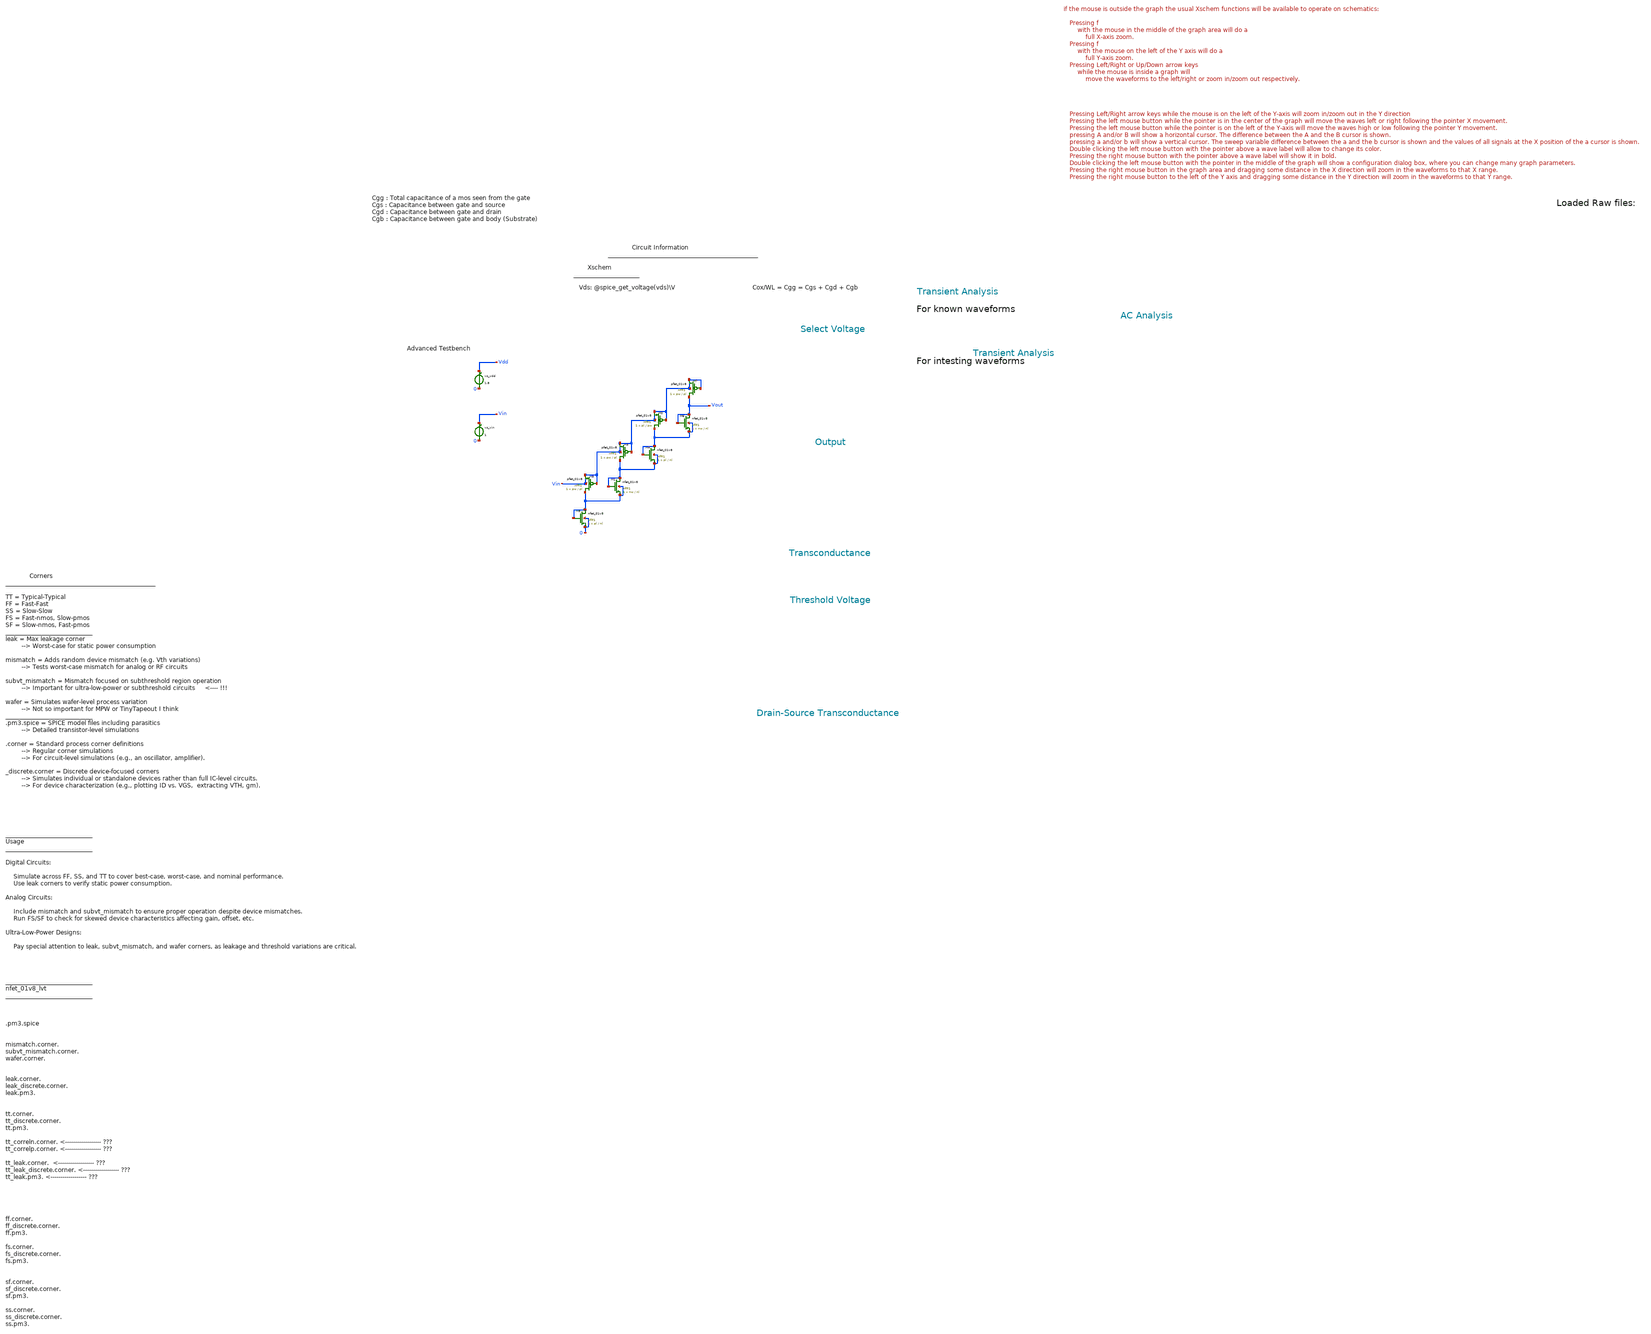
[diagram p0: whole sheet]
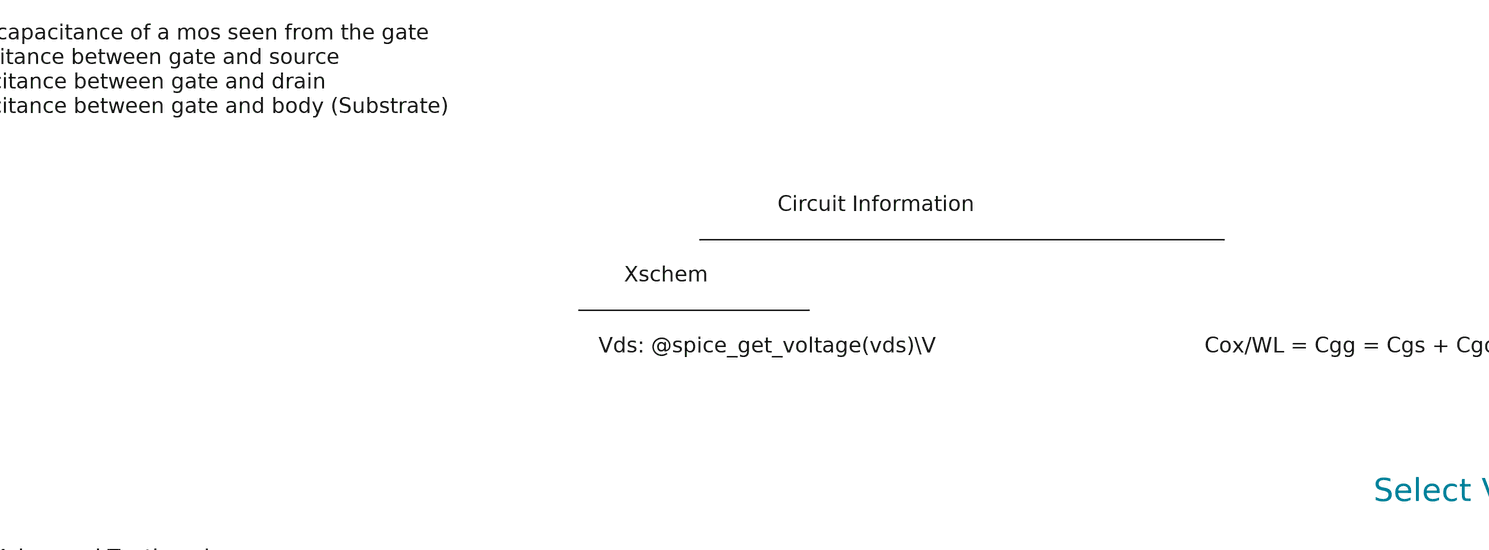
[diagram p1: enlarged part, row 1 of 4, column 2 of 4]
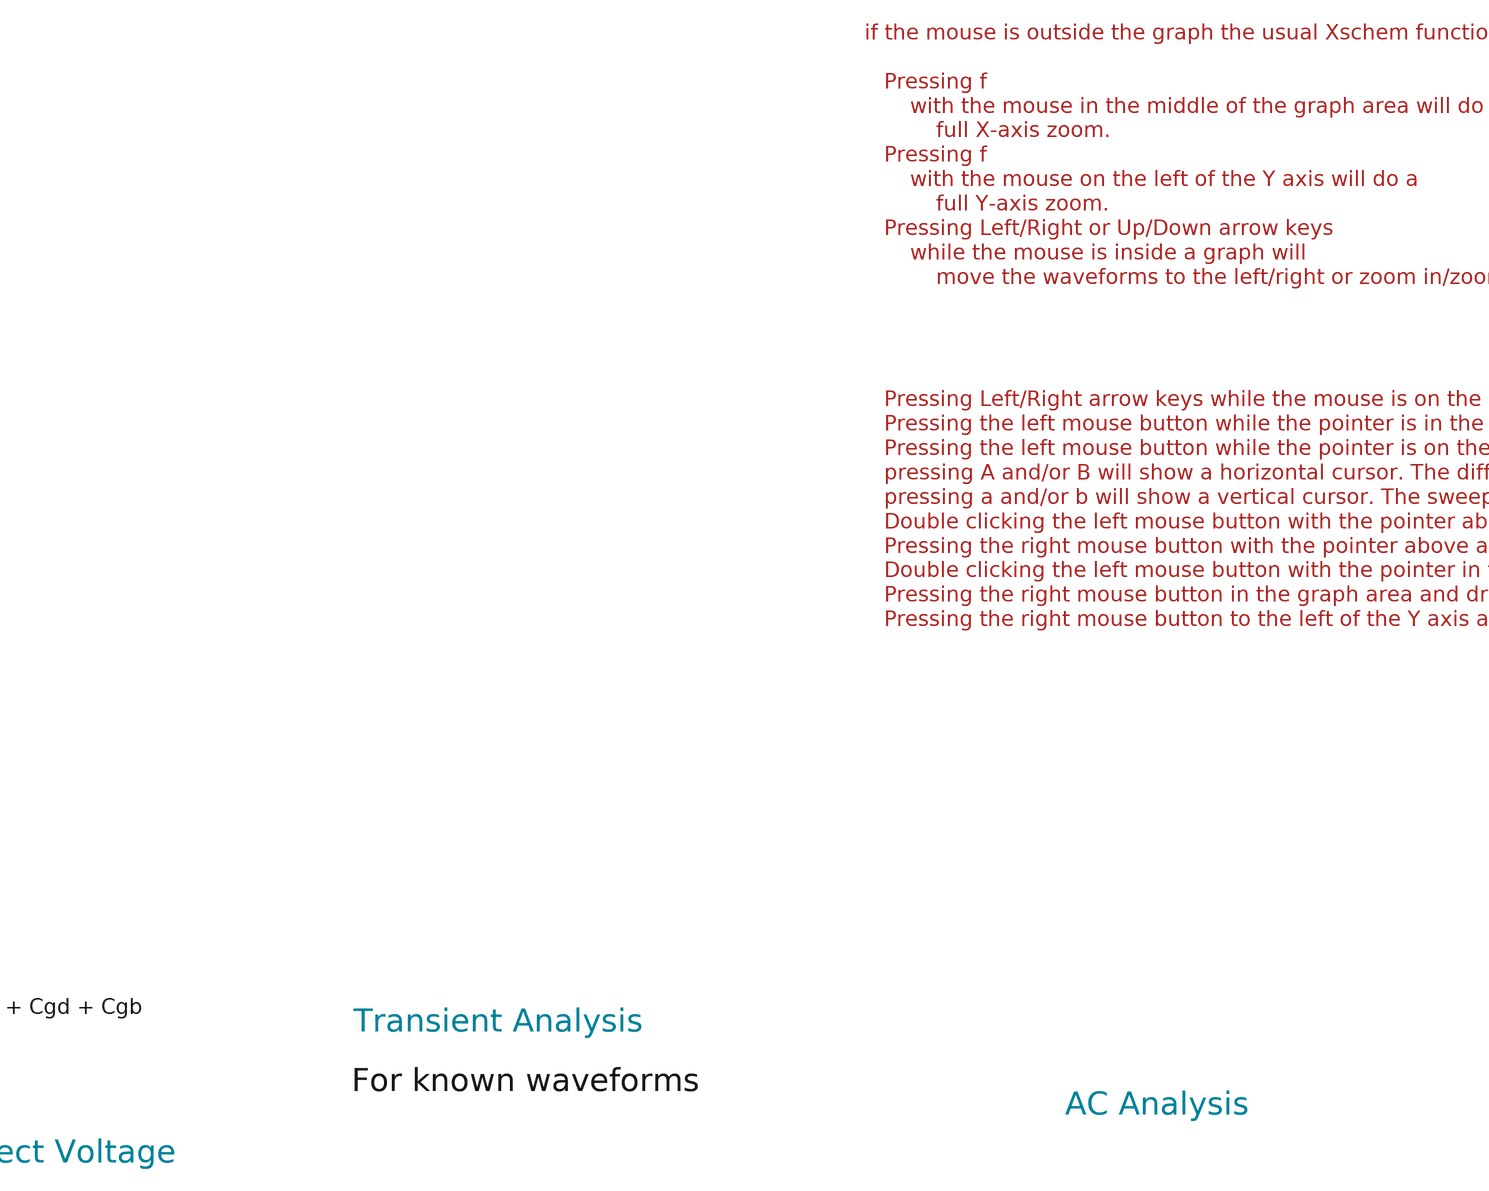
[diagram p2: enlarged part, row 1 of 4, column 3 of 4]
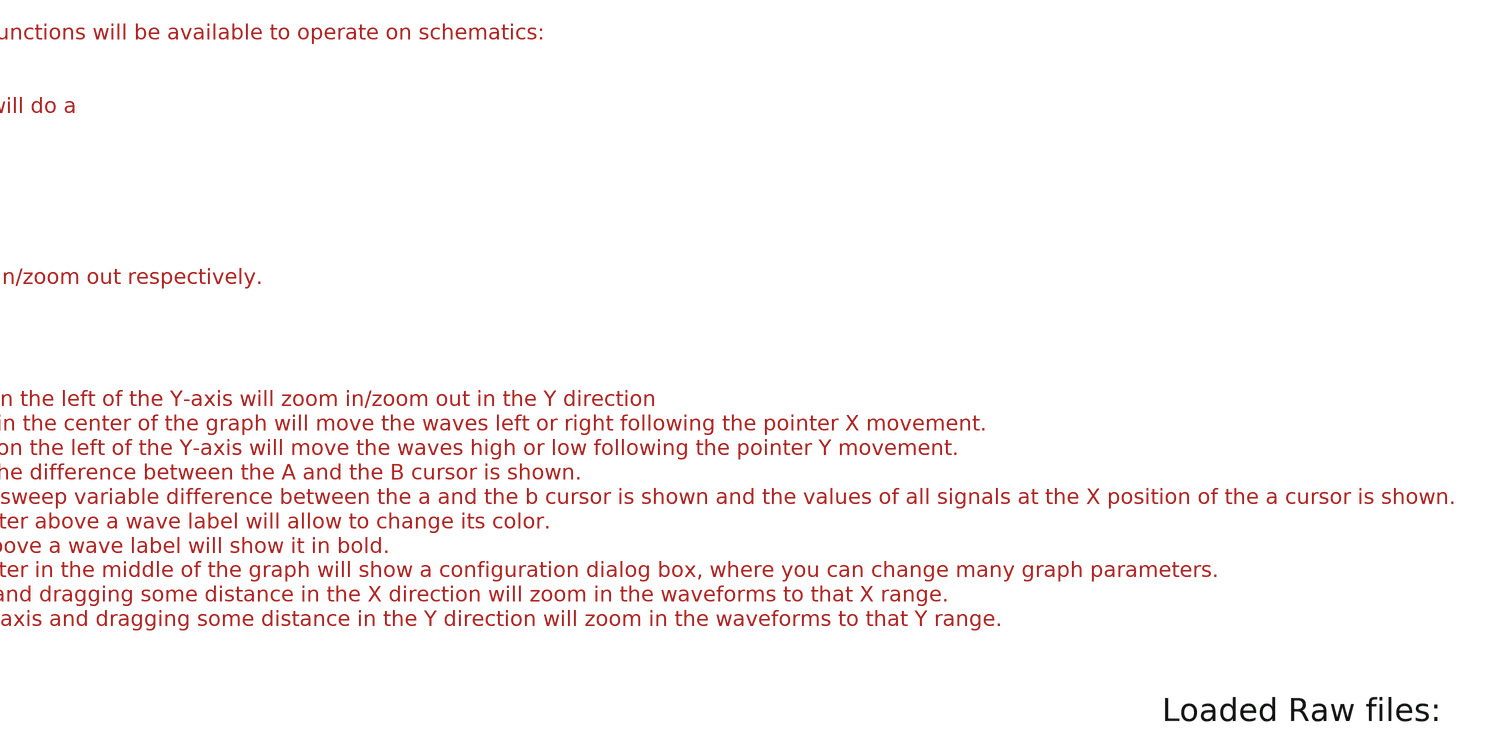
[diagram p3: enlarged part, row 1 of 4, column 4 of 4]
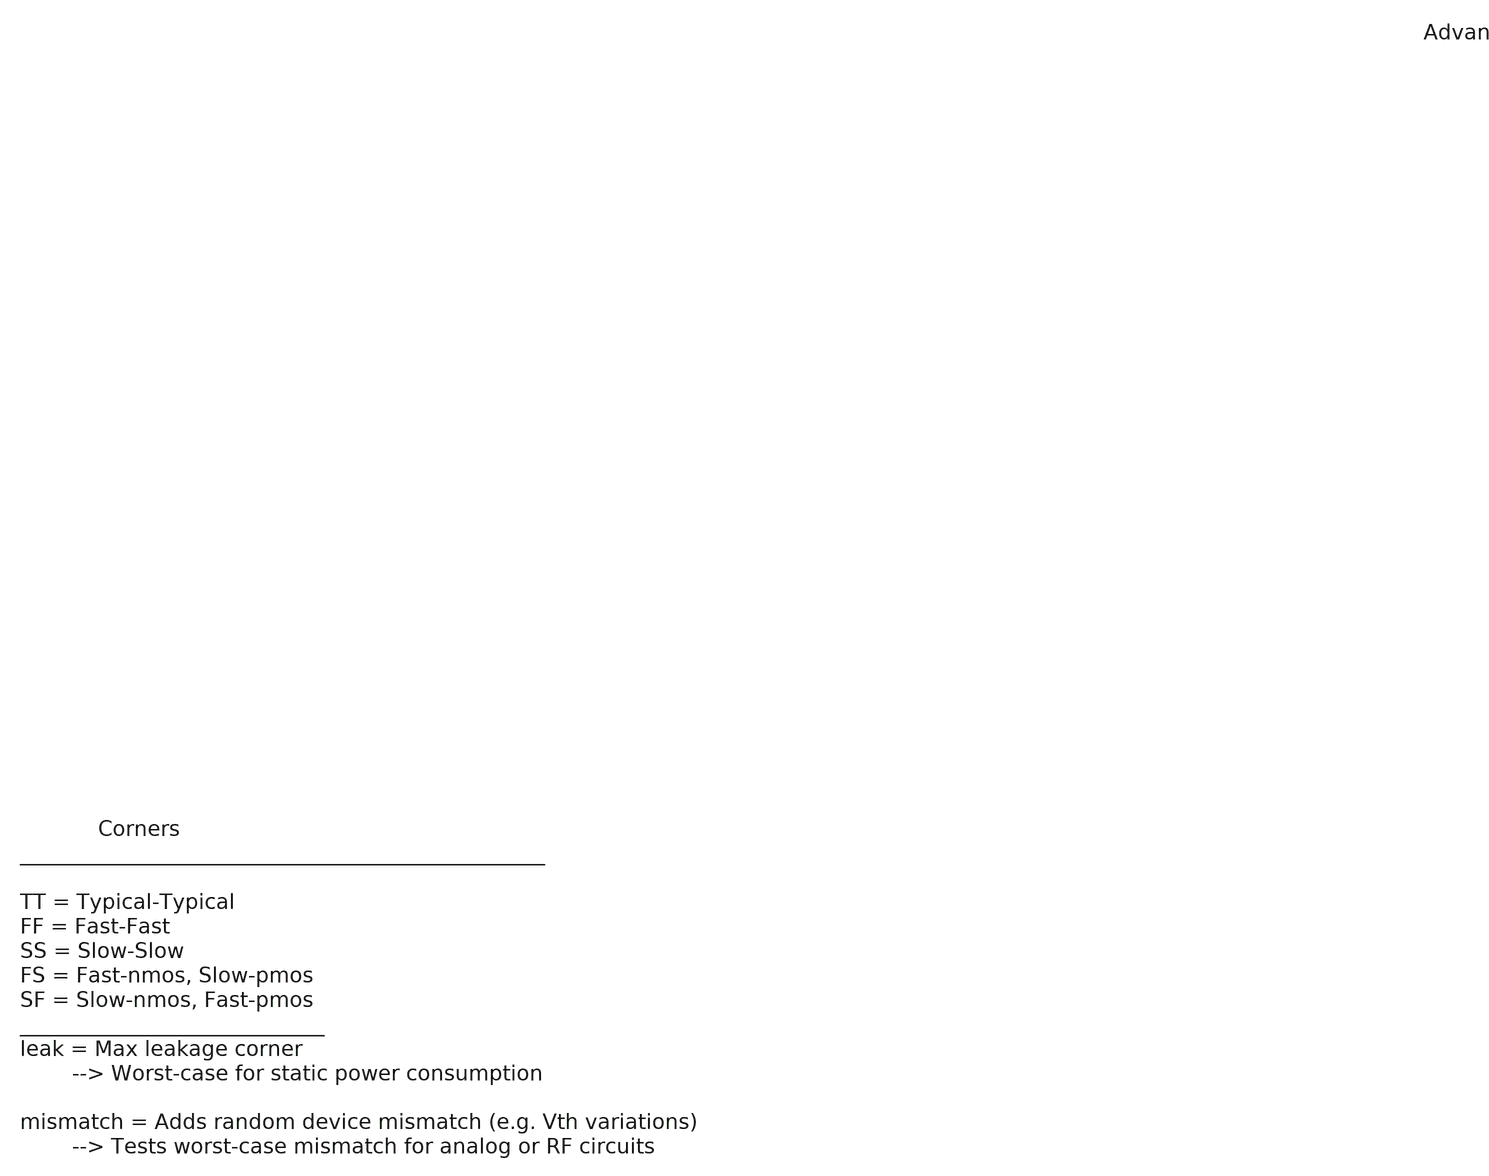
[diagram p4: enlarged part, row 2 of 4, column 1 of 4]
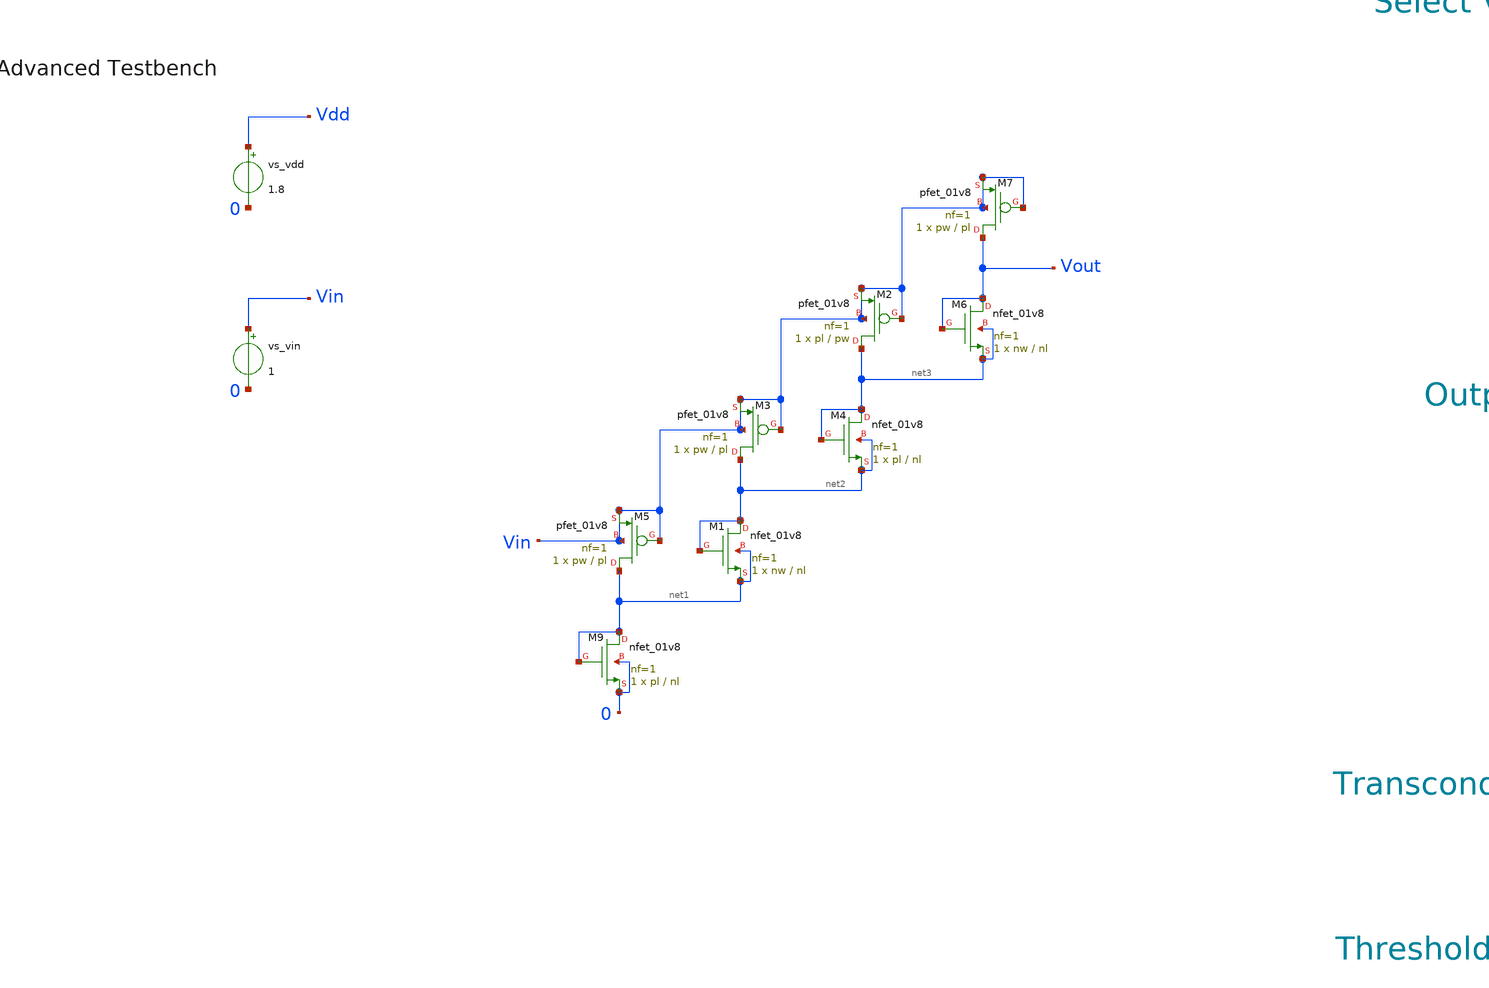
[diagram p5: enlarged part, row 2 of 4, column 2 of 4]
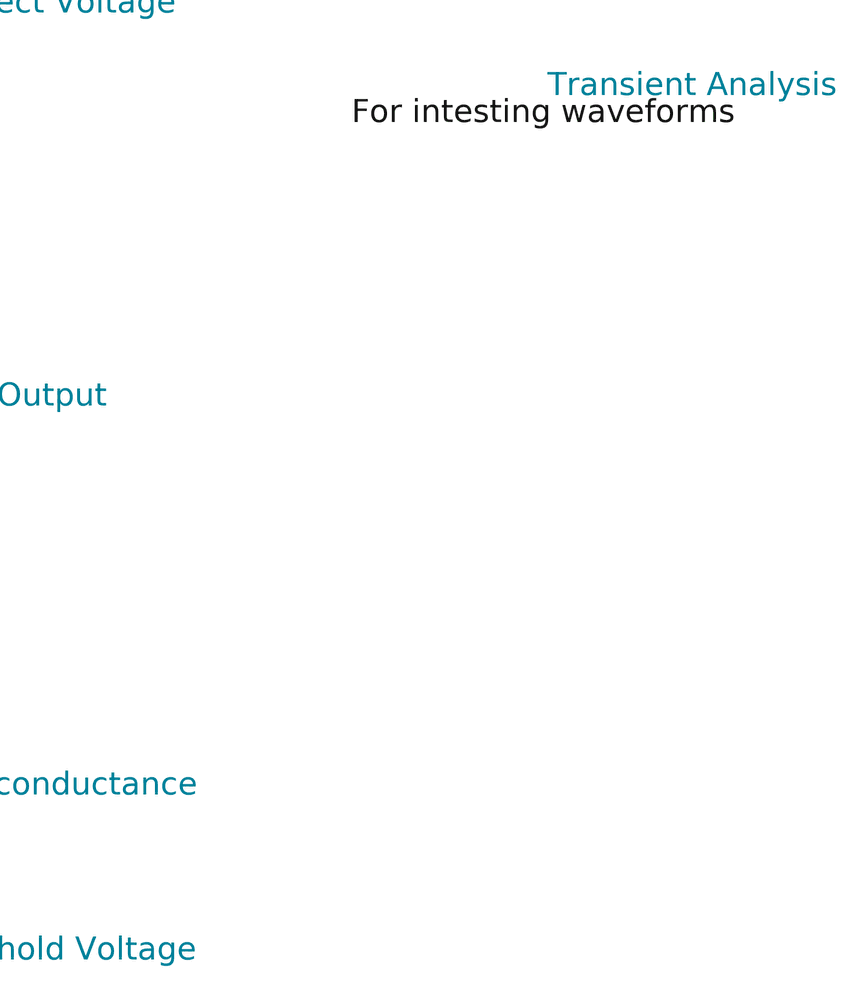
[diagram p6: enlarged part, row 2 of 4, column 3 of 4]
** sch_path: tt10-hdl/tt_um_test_commit/xschem/T0/mosRes/unknown_tb.sch
* Copyright (C) 1998-2024 Stefan Frederik Schippers
* This program is free software; you can redistribute it and/or modify
* it under the terms of the GNU General Public License as published by
* the Free Software Foundation; either version 2 of the License, or
* (at your option) any later version.
* This program is distributed in the hope that it will be useful,
* but WITHOUT ANY WARRANTY; without even the implied warranty of
* MERCHANTABILITY or FITNESS FOR A PARTICULAR PURPOSE.  See the
* GNU General Public License for more details.
* You should have received a copy of the GNU General Public License
* along with this program; if not, write to the Free Software
**.subckt unknown_tb
vs_vin Vin 0 1
vs_vdd Vdd 0 1.8
XM9 net1 net1 0 0 sky130_fd_pr__nfet_01v8 L=nl W=pl nf=1 ad='int((1 + 1)/2) * pl / 1 * 0.29' as='int((1 + 2)/2) * pl / 1 * 0.29'
+ pd='2*int((1 + 1)/2) * (pl / 1 + 0.29)' ps='2*int((1 + 2)/2) * (pl / 1 + 0.29)' nrd='0.29 / pl ' nrs='0.29 / pl '
+ sa=0 sb=0 sd=0 mult=1 m=1
XM7 Vout Vin Vin Vin sky130_fd_pr__pfet_01v8 L=pl W=pw nf=1 ad='int((nf+1)/2) * W/nf * 0.29' as='int((nf+2)/2) * W/nf * 0.29'
+ pd='2*int((nf+1)/2) * (W/nf + 0.29)' ps='2*int((nf+2)/2) * (W/nf + 0.29)' nrd='0.29 / W' nrs='0.29 / W'
+ sa=0 sb=0 sd=0 mult=1 m=1
XM1 net2 net2 net1 net1 sky130_fd_pr__nfet_01v8 L=nl W=nw nf=1 ad='int((1 + 1)/2) * nw / 1 * 0.29' as='int((1 + 2)/2) * nw / 1 * 0.29'
+ pd='2*int((1 + 1)/2) * (nw / 1 + 0.29)' ps='2*int((1 + 2)/2) * (nw / 1 + 0.29)' nrd='0.29 / nw ' nrs='0.29 / nw '
+ sa=0 sb=0 sd=0 mult=1 m=1
XM4 net3 net3 net2 net2 sky130_fd_pr__nfet_01v8 L=nl W=pl nf=1 ad='int((1 + 1)/2) * pl / 1 * 0.29' as='int((1 + 2)/2) * pl / 1 * 0.29'
+ pd='2*int((1 + 1)/2) * (pl / 1 + 0.29)' ps='2*int((1 + 2)/2) * (pl / 1 + 0.29)' nrd='0.29 / pl ' nrs='0.29 / pl '
+ sa=0 sb=0 sd=0 mult=1 m=1
XM6 Vout Vout net3 net3 sky130_fd_pr__nfet_01v8 L=nl W=nw nf=1 ad='int((1 + 1)/2) * nw / 1 * 0.29' as='int((1 + 2)/2) * nw / 1 * 0.29'
+ pd='2*int((1 + 1)/2) * (nw / 1 + 0.29)' ps='2*int((1 + 2)/2) * (nw / 1 + 0.29)' nrd='0.29 / nw ' nrs='0.29 / nw '
+ sa=0 sb=0 sd=0 mult=1 m=1
XM2 net3 Vin Vin Vin sky130_fd_pr__pfet_01v8 L=pw W=pl nf=1 ad='int((nf+1)/2) * W/nf * 0.29' as='int((nf+2)/2) * W/nf * 0.29'
+ pd='2*int((nf+1)/2) * (W/nf + 0.29)' ps='2*int((nf+2)/2) * (W/nf + 0.29)' nrd='0.29 / W' nrs='0.29 / W'
+ sa=0 sb=0 sd=0 mult=1 m=1
XM3 net2 Vin Vin Vin sky130_fd_pr__pfet_01v8 L=pl W=pw nf=1 ad='int((nf+1)/2) * W/nf * 0.29' as='int((nf+2)/2) * W/nf * 0.29'
+ pd='2*int((nf+1)/2) * (W/nf + 0.29)' ps='2*int((nf+2)/2) * (W/nf + 0.29)' nrd='0.29 / W' nrs='0.29 / W'
+ sa=0 sb=0 sd=0 mult=1 m=1
XM5 net1 Vin Vin Vin sky130_fd_pr__pfet_01v8 L=pl W=pw nf=1 ad='int((nf+1)/2) * W/nf * 0.29' as='int((nf+2)/2) * W/nf * 0.29'
+ pd='2*int((nf+1)/2) * (W/nf + 0.29)' ps='2*int((nf+2)/2) * (W/nf + 0.29)' nrd='0.29 / W' nrs='0.29 / W'
+ sa=0 sb=0 sd=0 mult=1 m=1
**** begin user architecture code



.temp 30
.param nw = 2
.param nl = 0.3
.param pw = 1
.param pl = 0.6

*.option gmin=5n
*.option scale=1e-6
*.option wnflag=1
.option savecurrents

.save all
.control
  save all alli

  save @m.xm1.msky130_fd_pr__nfet_01v8[gm]
  save @m.xm1.msky130_fd_pr__nfet_01v8[id]
  save @m.xm1.msky130_fd_pr__nfet_01v8_lvt[vgs]

  save @m.xm1.msky130_fd_pr__nfet_01v8[cgg]
  save @m.xm1.msky130_fd_pr__nfet_01v8[cgs]
  save @m.xm1.msky130_fd_pr__nfet_01v8[cgd]
  save @m.xm1.msky130_fd_pr__nfet_01v8[cgb]

  save @m.xm1.msky130_fd_pr__nfet_01v8[vds]
  save @m.xm1.msky130_fd_pr__nfet_01v8[vdsat]
  save @m.xm1.msky130_fd_pr__nfet_01v8[vth]


  save @m.xm1.msky130_fd_pr__nfet_01v8[leff]
  save @m.xm1.msky130_fd_pr__nfet_01v8[weff]
  save @m.xm1.msky130_fd_pr__nfet_01v8[gds]
  save @m.xm1.msky130_fd_pr__nfet_01v8[l]
  save @m.xm1.msky130_fd_pr__nfet_01v8[w]



  dc vs_vin 0 1.8  0.005
  *dc v_dev_vds 0 20u  10n
  write nmos_tb.raw


  op
  set appendwrite
  write nmos_tb.raw



  *tran 1n 5u
  *write nmos_tb.raw






  *quit 0




.endc





** opencircuitdesign pdks install
.lib $::SKYWATER_MODELS/sky130.lib.spice tt
.include $::SKYWATER_STDCELLS/sky130_fd_sc_hd.spice


**** end user architecture code
**.ends
.end
